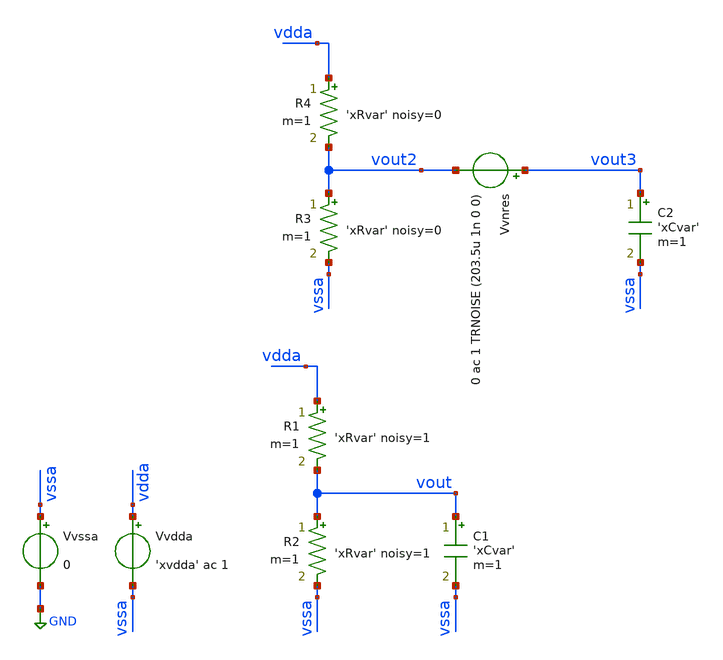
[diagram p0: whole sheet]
** sch_path: Running_transient_noise_in_ngspice/tb_kToverC_4.sch
**.subckt tb_kToverC_4
Vvdda vdda vssa 'xvdda' ac 1
Vvssa vssa GND 0
R2 vout vssa 'xRvar' noisy=1 m=1
R1 vdda vout 'xRvar' noisy=1 m=1
C1 vout vssa 'xCvar' m=1
R3 vout2 vssa 'xRvar' noisy=0 m=1
R4 vdda vout2 'xRvar' noisy=0 m=1
C2 vout3 vssa 'xCvar' m=1
Vvnres vout3 vout2 0 ac 1 TRNOISE (203.5u 1n 0 0)
**** begin user architecture code

** opencircuitdesign pdks install
* .lib /home/schippes/share/pdk/sky130A/libs.tech/combined/sky130.lib.spice tt
.lib /home/slice/pdk/SW130/share/pdk/sky130A/libs.tech/combined/sky130.lib.spice tt
*.lib /home/slice/pdk/SW130/share/pdk/sky130A/libs.tech/combined/sky130.lib.spice ss
*.lib /home/slice/pdk/SW130/share/pdk/sky130A/libs.tech/combined/sky130.lib.spice ff
*.lib /home/slice/pdk/SW130/share/pdk/sky130A/libs.tech/combined/sky130.lib.spice sf
*.lib /home/slice/pdk/SW130/share/pdk/sky130A/libs.tech/combined/sky130.lib.spice fs

* Parameters
.param xvdda = 1.8
.csparam xvdda_var = 'xvdda'
.param xtsim = 10u
.csparam xtsim_var = 'xtsim'
.param xvdrain = 1
.param xvgate = 0.57
.param xRvar = 10k
.param xCvar = 1p
.temp 27

  ** 1. DCOP analysis **
  ** must save the below for DCOP analysis to be back annotated onto the schematic
  *.option savecurrents
  * svt device
  .save
  +  @m.xdut.xm1.msky130_fd_pr__pfet_01v8[vgs]
  +  @m.xdut.xm1.msky130_fd_pr__pfet_01v8[vds]
  +  @m.xdut.xm1.msky130_fd_pr__pfet_01v8[vth]
  +  @m.xdut.xm1.msky130_fd_pr__pfet_01v8[gds]
  +  @m.xdut.xm1.msky130_fd_pr__pfet_01v8[gm]
  +  @m.xdut.xm1.msky130_fd_pr__pfet_01v8[id]
  +  @m.xdut.xm1.msky130_fd_pr__pfet_01v8[vdsat]

  .control

    * If you want to run the awk script on ac results
    save all
    * If you want to run histogram analysis on transient noise results (octave script set up when
+ only vout3 is saved)
    *save v(vout3)
    * If you only want to view transient results
    *save v(vout3) v(vout)
    * If you want to view transient / ac results
    *save v(vout3) v(vout) onoise_spectrum onoise_total


** 1. DCOP ANALYSIS **

  op
  remzerovec
  write dcop.raw

** 2. TRAN ANALYSIS **

  tran 1n $&xtsim_var
  remzerovec
  write tran.raw

  * only required if post processing stdev / mean in octave
  *set filetype=ascii
  *remzerovec
  *write tran_data_ascii.raw

** 3. AC NOISE ANALYSIS **

  let xfmax = 500Meg;

  noise v(vout) Vvdda dec 10 1e3 $&xfmax 1
  print v(onoise_total)
  setplot noise1
  set filetype=binary
  remzerovec
  write noise_density.raw
*  plot onoise_spectrum
  let vnoise_op_int = sqrt(integ(onoise_spectrum*onoise_spectrum))
*  plot vnoise_op_int xlog

  setplot noise2
  set filetype=ascii
  remzerovec
  write integrated_noise.raw

setplot

*quit 0
.endc




**** end user architecture code
**.ends
.GLOBAL GND
.end
